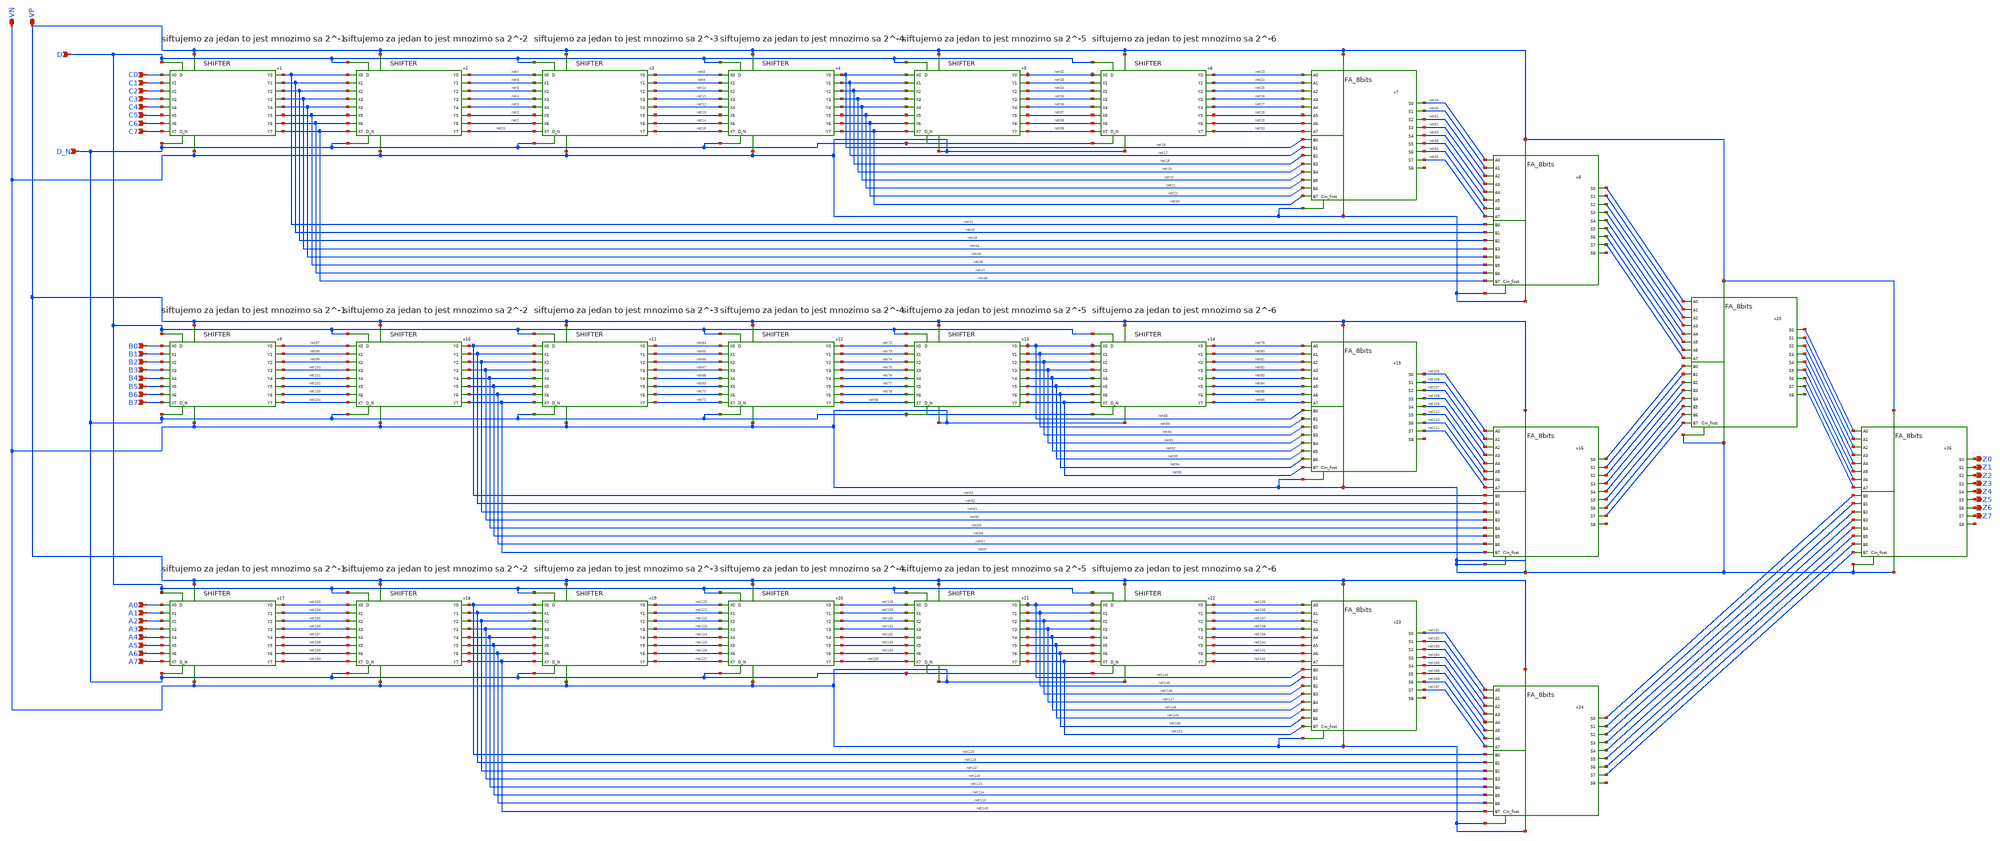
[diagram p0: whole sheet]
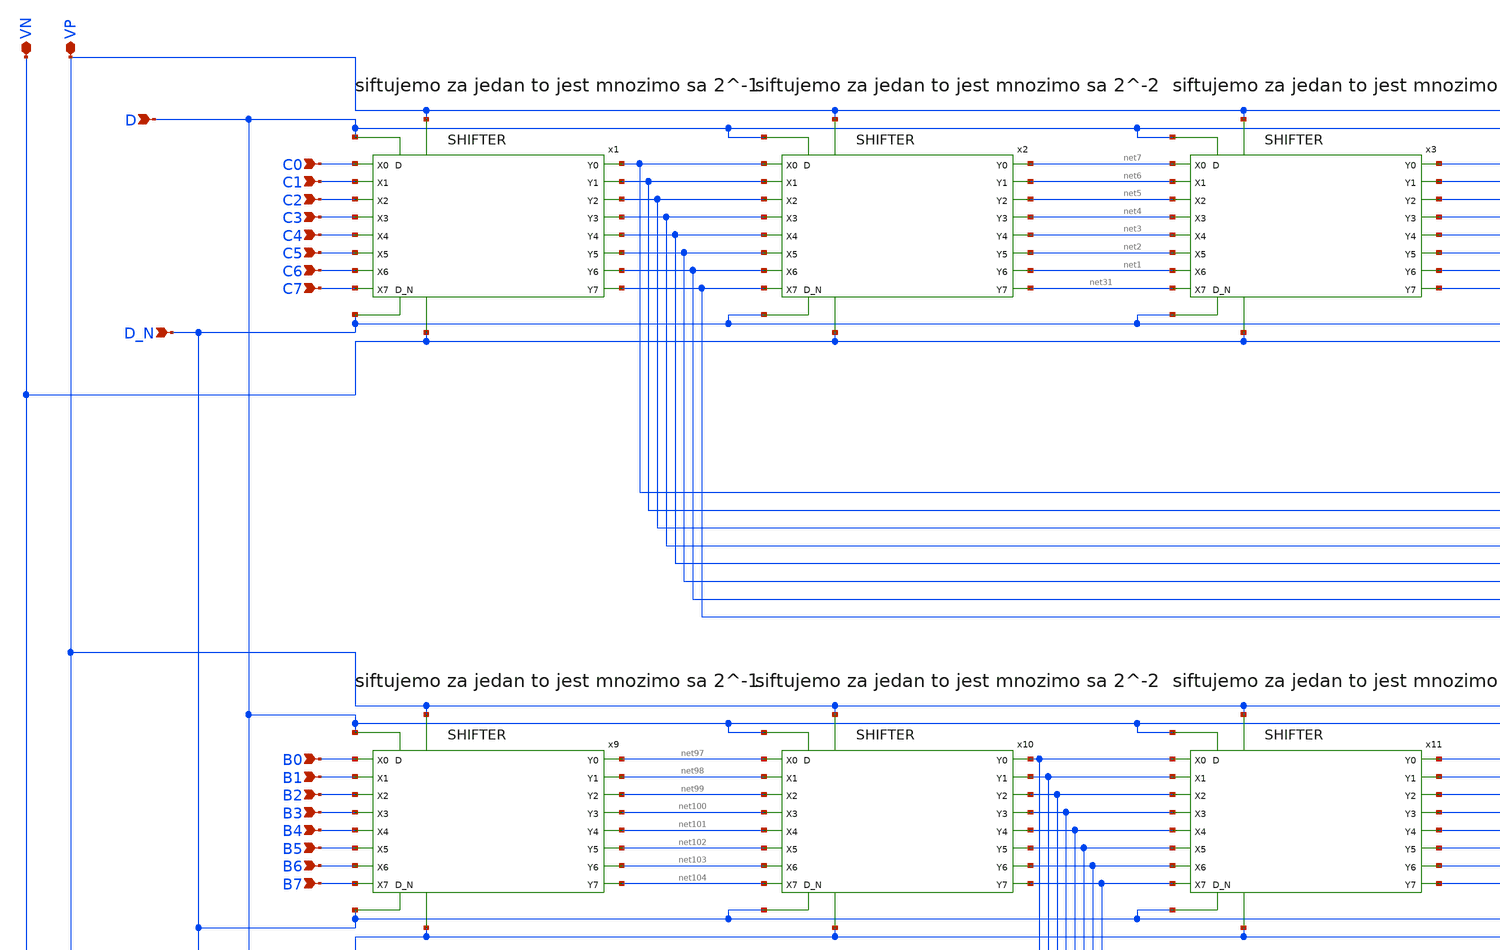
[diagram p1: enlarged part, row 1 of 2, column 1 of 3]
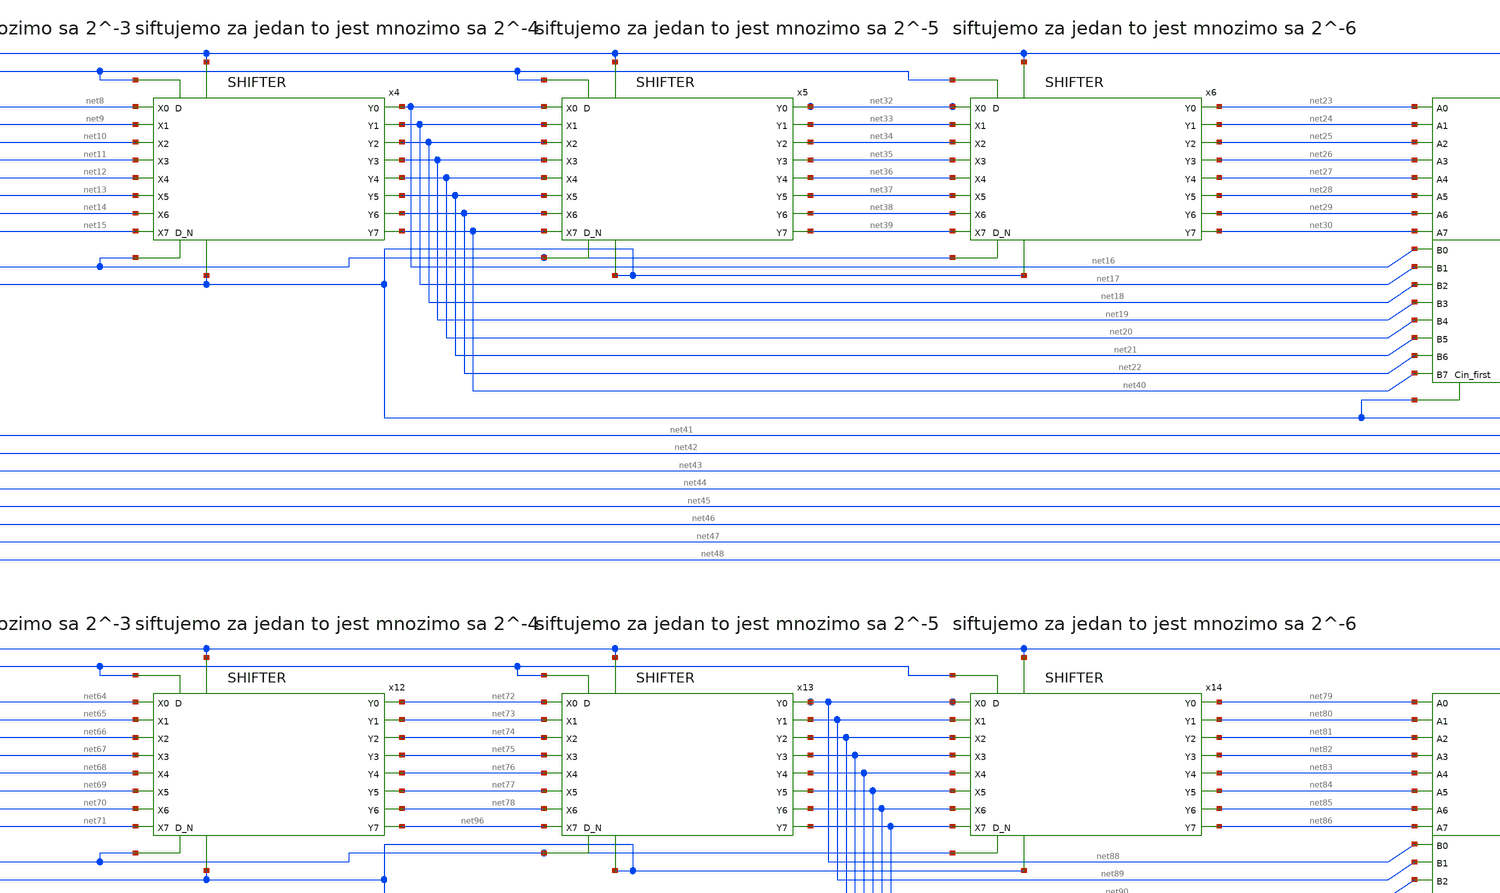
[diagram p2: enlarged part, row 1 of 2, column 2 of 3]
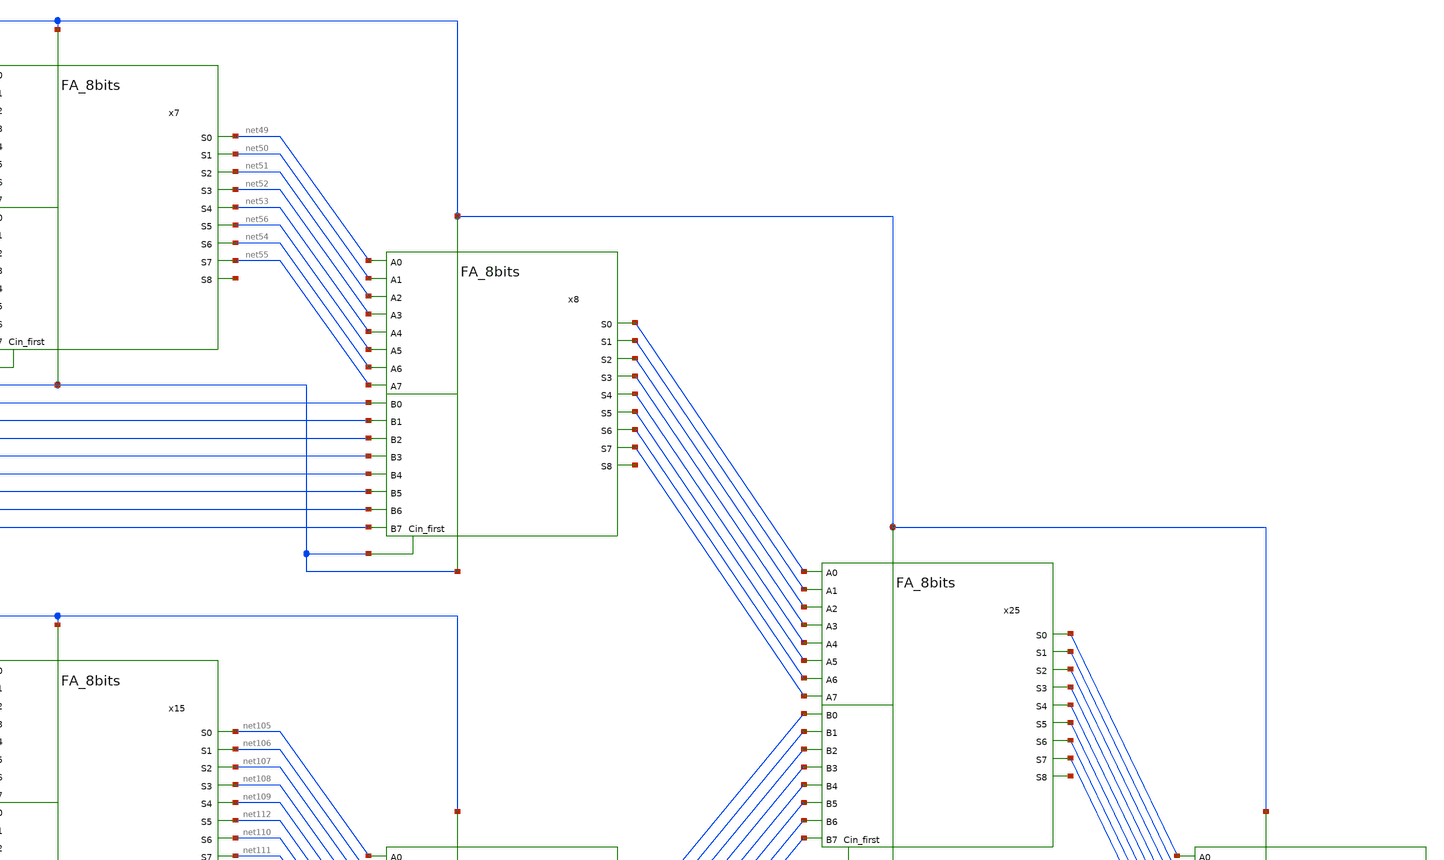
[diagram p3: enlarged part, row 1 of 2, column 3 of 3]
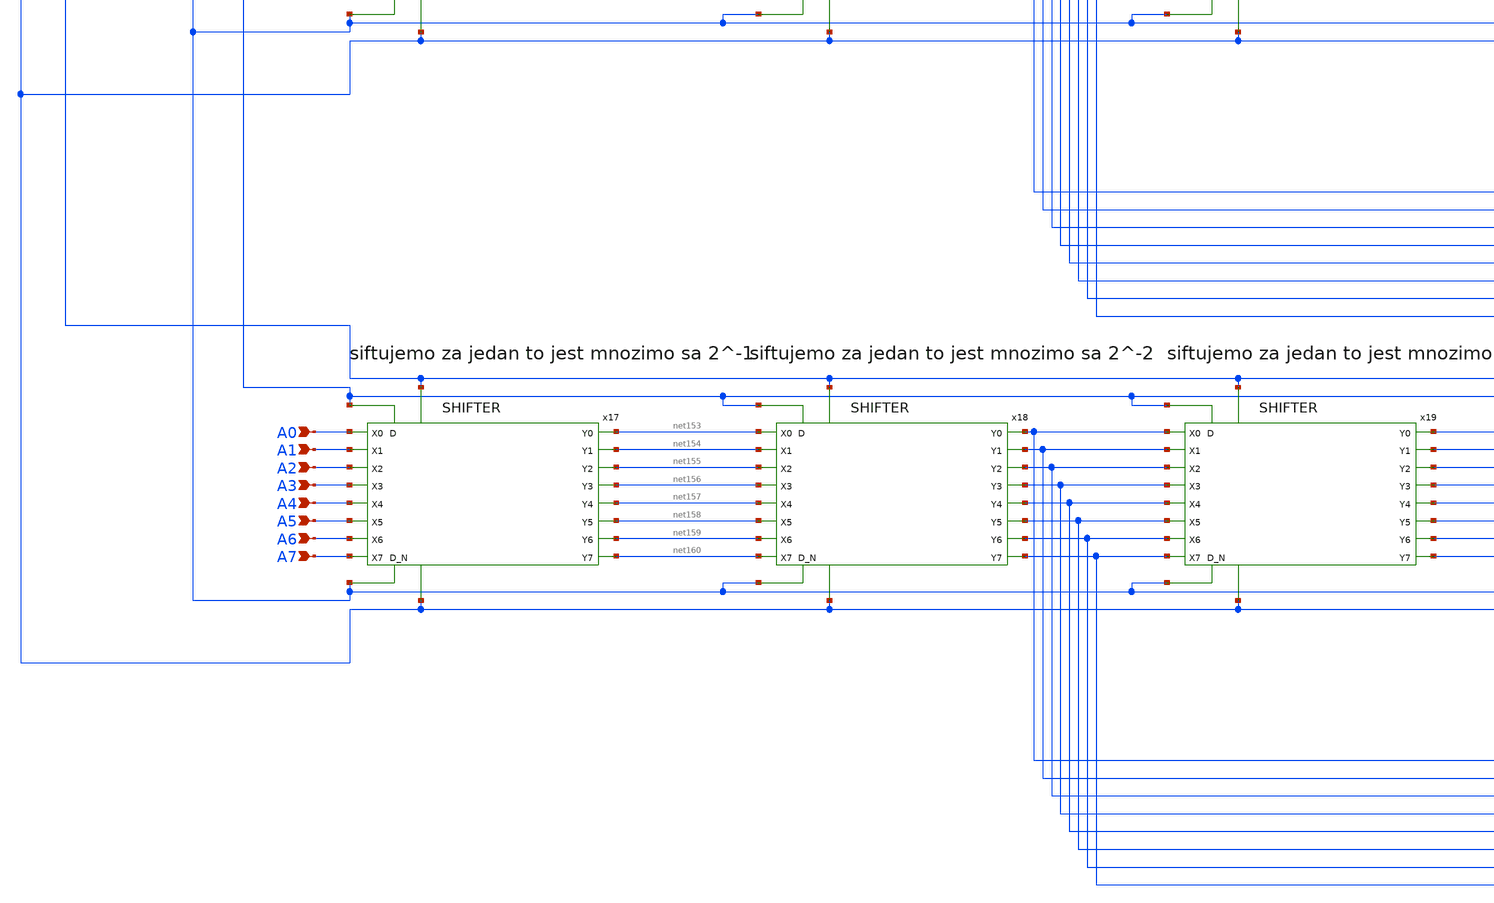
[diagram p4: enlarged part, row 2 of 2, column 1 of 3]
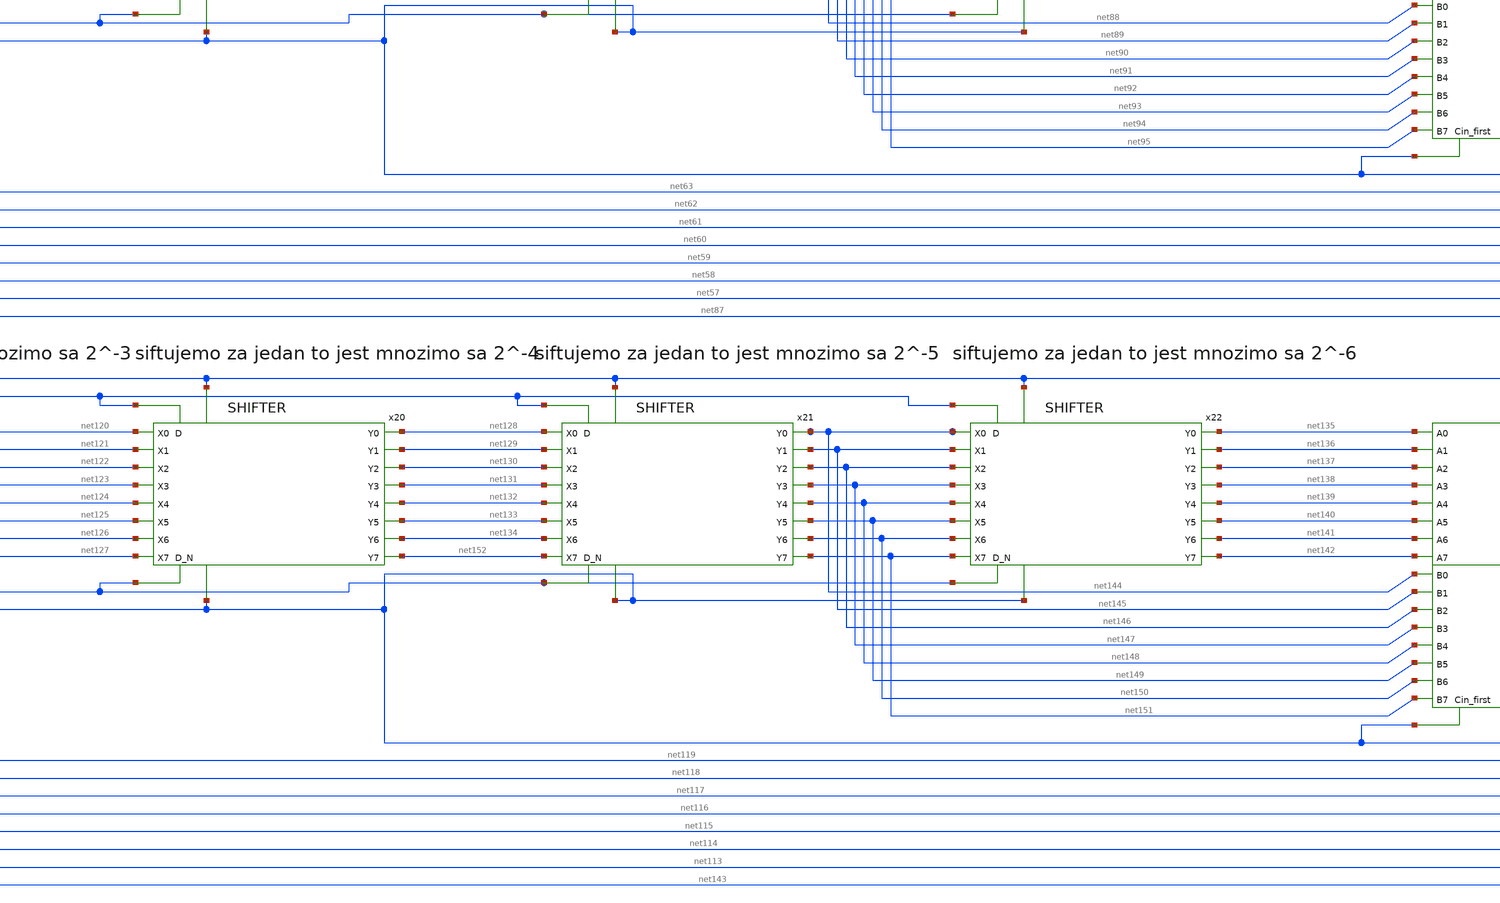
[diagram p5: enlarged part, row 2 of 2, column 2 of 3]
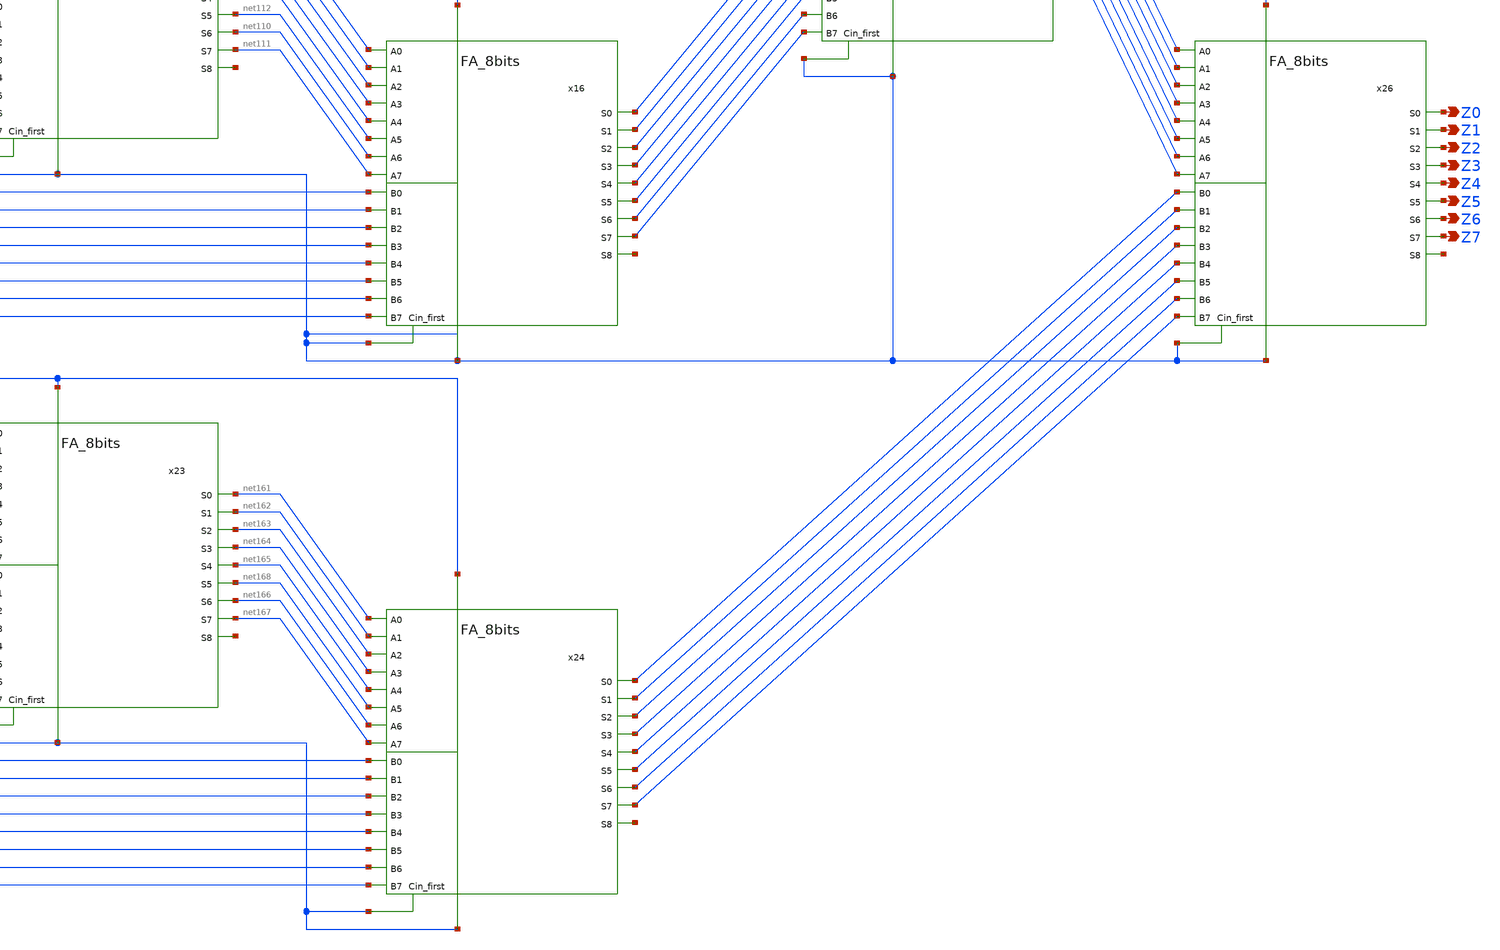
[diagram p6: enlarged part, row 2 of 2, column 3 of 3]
** sch_path: projekat_spice/layout/fir/FIR.sch
* projekat_spice/layout/fa/FA.sym:
* Copyright 2022 Stefan Frederik Schippers
* Licensed under the Apache License, Version 2.0 (the "License");
**.subckt FIR C0 C1 C2 C3 C4 C5 C6 C7 VP VN D D_N Z0 Z1 Z2 Z3 Z4 Z5 Z6 Z7 B0 B1 B2 B3 B4 B5 B6 B7 A0
*+ A1 A2 A3 A4 A5 A6 A7
*.ipin C0
*.ipin C1
*.ipin C2
*.ipin C3
*.ipin C4
*.ipin C5
*.ipin C6
*.ipin C7
*.iopin VP
*.iopin VN
*.ipin D
*.ipin D_N
*.opin Z0
*.opin Z1
*.opin Z2
*.opin Z3
*.opin Z4
*.opin Z5
*.opin Z6
*.opin Z7
*.ipin B0
*.ipin B1
*.ipin B2
*.ipin B3
*.ipin B4
*.ipin B5
*.ipin B6
*.ipin B7
*.ipin A0
*.ipin A1
*.ipin A2
*.ipin A3
*.ipin A4
*.ipin A5
*.ipin A6
*.ipin A7
x1 C0 net41 net42 C1 net43 C2 C3 net44 net45 C4 C5 net46 net47 C6 net48 C7 D D_N VP VN SHIFTER
x2 net41 net7 net6 net42 net5 net43 net44 net4 net3 net45 net46 net2 net1 net47 net31 net48 D D_N VP
+ VN SHIFTER
x3 net7 net8 net9 net6 net10 net5 net4 net11 net12 net3 net2 net13 net14 net1 net15 net31 D D_N VP
+ VN SHIFTER
x4 net8 net16 net17 net9 net18 net10 net11 net19 net20 net12 net13 net21 net22 net14 net40 net15 D
+ D_N VP VN SHIFTER
x5 net16 net32 net33 net17 net34 net18 net19 net35 net36 net20 net21 net37 net38 net22 net39 net40 D
+ D_N VP VN SHIFTER
x6 net32 net23 net24 net33 net25 net34 net35 net26 net27 net36 net37 net28 net29 net38 net30 net39 D
+ D_N VP VN SHIFTER
x7 net16 net17 net18 net19 net20 net21 net22 net40 net23 net24 net25 net26 net27 net28 net29 net30
+ net49 net50 net51 net52 net53 net56 net54 net55 net201 VN VP VN FA_8bits
x8 net41 net42 net43 net44 net45 net46 net47 net48 net49 net50 net51 net52 net53 net56 net54 net55
+ net169 net170 net172 net171 net173 net174 net175 net176 net202 VN VP VN FA_8bits
x9 B0 net97 net98 B1 net99 B2 B3 net100 net101 B4 B5 net102 net103 B6 net104 B7 D D_N VP VN SHIFTER
x10 net97 net63 net62 net98 net61 net99 net100 net60 net59 net101 net102 net58 net57 net103 net87
+ net104 D D_N VP VN SHIFTER
x11 net63 net64 net65 net62 net66 net61 net60 net67 net68 net59 net58 net69 net70 net57 net71 net87
+ D D_N VP VN SHIFTER
x12 net64 net72 net73 net65 net74 net66 net67 net75 net76 net68 net69 net77 net78 net70 net96 net71
+ D D_N VP VN SHIFTER
x13 net72 net88 net89 net73 net90 net74 net75 net91 net92 net76 net77 net93 net94 net78 net95 net96
+ D D_N VP VN SHIFTER
x14 net88 net79 net80 net89 net81 net90 net91 net82 net83 net92 net93 net84 net85 net94 net86 net95
+ D D_N VP VN SHIFTER
x15 net88 net89 net90 net91 net92 net93 net94 net95 net79 net80 net81 net82 net83 net84 net85 net86
+ net105 net106 net107 net108 net109 net112 net110 net111 net203 VN VP VN FA_8bits
x16 net63 net62 net61 net60 net59 net58 net57 net87 net105 net106 net107 net108 net109 net112 net110
+ net111 net177 net178 net179 net180 net181 net182 net183 net184 net204 VN VP VN FA_8bits
x17 A0 net153 net154 A1 net155 A2 A3 net156 net157 A4 A5 net158 net159 A6 net160 A7 D D_N VP VN
+ SHIFTER
x18 net153 net119 net118 net154 net117 net155 net156 net116 net115 net157 net158 net114 net113
+ net159 net143 net160 D D_N VP VN SHIFTER
x19 net119 net120 net121 net118 net122 net117 net116 net123 net124 net115 net114 net125 net126
+ net113 net127 net143 D D_N VP VN SHIFTER
x20 net120 net128 net129 net121 net130 net122 net123 net131 net132 net124 net125 net133 net134
+ net126 net152 net127 D D_N VP VN SHIFTER
x21 net128 net144 net145 net129 net146 net130 net131 net147 net148 net132 net133 net149 net150
+ net134 net151 net152 D D_N VP VN SHIFTER
x22 net144 net135 net136 net145 net137 net146 net147 net138 net139 net148 net149 net140 net141
+ net150 net142 net151 D D_N VP VN SHIFTER
x23 net144 net145 net146 net147 net148 net149 net150 net151 net135 net136 net137 net138 net139
+ net140 net141 net142 net161 net162 net163 net164 net165 net168 net166 net167 net205 VN VP VN FA_8bits
x24 net119 net118 net117 net116 net115 net114 net113 net143 net161 net162 net163 net164 net165
+ net168 net166 net167 net193 net194 net195 net196 net197 net198 net199 net200 net206 VN VP VN FA_8bits
x25 net177 net178 net179 net180 net181 net182 net183 net184 net169 net170 net172 net171 net173
+ net174 net175 net176 net185 net186 net187 net188 net189 net190 net191 net192 net207 VN VP VN FA_8bits
x26 net193 net194 net195 net196 net197 net198 net199 net200 net185 net186 net187 net188 net189
+ net190 net191 net192 Z0 Z1 Z2 Z3 Z4 Z5 Z6 Z7 net208 VN VP VN FA_8bits
**.ends

* expanding   symbol:  /home/mihailo/projekat_sky130/projekat_layout/shifter/SHIFTER.sym # of
*+ pins=20
** sym_path: projekat_spice/layout/shifter/SHIFTER.sym
** sch_path: projekat_spice/layout/shifter/SHIFTER.sch
.subckt SHIFTER X0 Y0 Y1 X1 Y2 X2 X3 Y3 Y4 X4 X5 Y5 Y6 X6 Y7 X7 D D_N VP VN
*.iopin VP
*.iopin VN
*.ipin X0
*.ipin X1
*.ipin X2
*.ipin X3
*.ipin X4
*.ipin X5
*.ipin X6
*.ipin X7
*.ipin D
*.ipin D_N
*.opin Y0
*.opin Y1
*.opin Y2
*.opin Y3
*.opin Y4
*.opin Y5
*.opin Y6
*.opin Y7
X1 X0 D net1 VP VN AND
X3 D_N X1 Y0 VP VN AND
X4 X1 D net2 VP VN AND
X5 D_N X2 net3 VP VN AND
X6 X2 D net4 VP VN AND
X7 D_N X3 net5 VP VN AND
X8 X3 D net6 VP VN AND
X9 D_N X4 net7 VP VN AND
X10 X4 D net8 VP VN AND
X11 D_N X5 net9 VP VN AND
X12 X5 D net10 VP VN AND
X13 D_N X6 net11 VP VN AND
X14 X6 D Y7 VP VN AND
X15 D_N X7 net12 VP VN AND
X2 net1 net3 Y1 VP VN OR
X16 net2 net5 Y2 VP VN OR
X17 net4 net7 Y3 VP VN OR
X18 net6 net9 Y4 VP VN OR
X19 net8 net11 Y5 VP VN OR
X20 net10 net12 Y6 VP VN OR
.ends


* expanding   symbol:  /home/mihailo/projekat_sky130/projekat_layout/fa_8bits/FA_8bits.sym # of
*+ pins=28
** sym_path: projekat_spice/layout/fa_8bits/FA_8bits.sym
** sch_path: projekat_spice/layout/fa_8bits/FA_8bits.sch
.subckt FA_8bits B0 B1 B2 B3 B4 B5 B6 B7 A0 A1 A2 A3 A4 A5 A6 A7 S0 S1 S2 S3 S4 S5 S6 S7 S8
+ Cin_first VP VN
*.ipin A0
*.ipin B0
*.ipin A1
*.ipin B1
*.opin S0
*.opin S1
*.iopin VP
*.iopin VN
*.ipin Cin_first
*.ipin A2
*.ipin B2
*.opin S2
*.ipin A3
*.ipin B3
*.opin S3
*.ipin A4
*.ipin B4
*.opin S4
*.ipin A5
*.ipin B5
*.opin S5
*.ipin A6
*.ipin B6
*.opin S6
*.opin S7
*.ipin A7
*.ipin B7
*.opin S8
X1 A0 B0 Cin_first net1 S0 VP VN FA
X2 A1 B1 net1 net2 S1 VP VN FA
X3 A2 B2 net2 net3 S2 VP VN FA
X4 A3 B3 net3 net4 S3 VP VN FA
X5 A4 B4 net4 net5 S4 VP VN FA
X6 A5 B5 net5 net6 S5 VP VN FA
X7 A6 B6 net6 net7 S6 VP VN FA
X8 A7 B7 net7 S8 S7 VP VN FA
.ends


* expanding   symbol:  /home/mihailo/projekat_sky130/projekat_layout/and/AND.sym # of pins=5
** sym_path: projekat_spice/layout/and/AND.sym
** sch_path: projekat_spice/layout/and/AND.sch
.subckt AND A B X VP VN
*.ipin A
*.ipin B
*.iopin VN
*.iopin VP
*.opin X
XM1 net1 A net2 VN sky130_fd_pr__nfet_01v8 L=0.15 W=1 nf=1 ad='int((nf+1)/2) * W/nf * 0.29' as='int((nf+2)/2) * W/nf * 0.29'
+ pd='2*int((nf+1)/2) * (W/nf + 0.29)' ps='2*int((nf+2)/2) * (W/nf + 0.29)' nrd='0.29 / W' nrs='0.29 / W'
+ sa=0 sb=0 sd=0 mult=1 m=1
XM2 net1 A VP VP sky130_fd_pr__pfet_01v8 L=0.15 W=1 nf=1 ad='int((nf+1)/2) * W/nf * 0.29' as='int((nf+2)/2) * W/nf * 0.29'
+ pd='2*int((nf+1)/2) * (W/nf + 0.29)' ps='2*int((nf+2)/2) * (W/nf + 0.29)' nrd='0.29 / W' nrs='0.29 / W'
+ sa=0 sb=0 sd=0 mult=1 m=1
XM3 net1 B VP VP sky130_fd_pr__pfet_01v8 L=0.15 W=1 nf=1 ad='int((nf+1)/2) * W/nf * 0.29' as='int((nf+2)/2) * W/nf * 0.29'
+ pd='2*int((nf+1)/2) * (W/nf + 0.29)' ps='2*int((nf+2)/2) * (W/nf + 0.29)' nrd='0.29 / W' nrs='0.29 / W'
+ sa=0 sb=0 sd=0 mult=1 m=1
XM4 net2 B VN VN sky130_fd_pr__nfet_01v8 L=0.15 W=1 nf=1 ad='int((nf+1)/2) * W/nf * 0.29' as='int((nf+2)/2) * W/nf * 0.29'
+ pd='2*int((nf+1)/2) * (W/nf + 0.29)' ps='2*int((nf+2)/2) * (W/nf + 0.29)' nrd='0.29 / W' nrs='0.29 / W'
+ sa=0 sb=0 sd=0 mult=1 m=1
XM5 X net1 VN VN sky130_fd_pr__nfet_01v8 L=0.15 W=1 nf=1 ad='int((nf+1)/2) * W/nf * 0.29' as='int((nf+2)/2) * W/nf * 0.29'
+ pd='2*int((nf+1)/2) * (W/nf + 0.29)' ps='2*int((nf+2)/2) * (W/nf + 0.29)' nrd='0.29 / W' nrs='0.29 / W'
+ sa=0 sb=0 sd=0 mult=1 m=1
XM6 X net1 VP VP sky130_fd_pr__pfet_01v8 L=0.15 W=1 nf=1 ad='int((nf+1)/2) * W/nf * 0.29' as='int((nf+2)/2) * W/nf * 0.29'
+ pd='2*int((nf+1)/2) * (W/nf + 0.29)' ps='2*int((nf+2)/2) * (W/nf + 0.29)' nrd='0.29 / W' nrs='0.29 / W'
+ sa=0 sb=0 sd=0 mult=1 m=1
.ends


* expanding   symbol:  /home/mihailo/projekat_sky130/projekat_layout/or/OR.sym # of pins=5
** sym_path: projekat_spice/layout/or/OR.sym
** sch_path: projekat_spice/layout/or/OR.sch
.subckt OR A B X VP VN
*.opin X
*.ipin A
*.ipin B
*.iopin VP
*.iopin VN
XM1 net2 A VN VN sky130_fd_pr__nfet_01v8 L=0.15 W=1 nf=1 ad='int((nf+1)/2) * W/nf * 0.29' as='int((nf+2)/2) * W/nf * 0.29'
+ pd='2*int((nf+1)/2) * (W/nf + 0.29)' ps='2*int((nf+2)/2) * (W/nf + 0.29)' nrd='0.29 / W' nrs='0.29 / W'
+ sa=0 sb=0 sd=0 mult=1 m=1
XM2 net1 A VP VP sky130_fd_pr__pfet_01v8 L=0.15 W=1 nf=1 ad='int((nf+1)/2) * W/nf * 0.29' as='int((nf+2)/2) * W/nf * 0.29'
+ pd='2*int((nf+1)/2) * (W/nf + 0.29)' ps='2*int((nf+2)/2) * (W/nf + 0.29)' nrd='0.29 / W' nrs='0.29 / W'
+ sa=0 sb=0 sd=0 mult=1 m=1
XM3 net2 B net1 VP sky130_fd_pr__pfet_01v8 L=0.15 W=1 nf=1 ad='int((nf+1)/2) * W/nf * 0.29' as='int((nf+2)/2) * W/nf * 0.29'
+ pd='2*int((nf+1)/2) * (W/nf + 0.29)' ps='2*int((nf+2)/2) * (W/nf + 0.29)' nrd='0.29 / W' nrs='0.29 / W'
+ sa=0 sb=0 sd=0 mult=1 m=1
XM4 net2 B VN VN sky130_fd_pr__nfet_01v8 L=0.15 W=1 nf=1 ad='int((nf+1)/2) * W/nf * 0.29' as='int((nf+2)/2) * W/nf * 0.29'
+ pd='2*int((nf+1)/2) * (W/nf + 0.29)' ps='2*int((nf+2)/2) * (W/nf + 0.29)' nrd='0.29 / W' nrs='0.29 / W'
+ sa=0 sb=0 sd=0 mult=1 m=1
XM5 X net2 VN VN sky130_fd_pr__nfet_01v8 L=0.15 W=1 nf=1 ad='int((nf+1)/2) * W/nf * 0.29' as='int((nf+2)/2) * W/nf * 0.29'
+ pd='2*int((nf+1)/2) * (W/nf + 0.29)' ps='2*int((nf+2)/2) * (W/nf + 0.29)' nrd='0.29 / W' nrs='0.29 / W'
+ sa=0 sb=0 sd=0 mult=1 m=1
XM6 X net2 VP VP sky130_fd_pr__pfet_01v8 L=0.15 W=1 nf=1 ad='int((nf+1)/2) * W/nf * 0.29' as='int((nf+2)/2) * W/nf * 0.29'
+ pd='2*int((nf+1)/2) * (W/nf + 0.29)' ps='2*int((nf+2)/2) * (W/nf + 0.29)' nrd='0.29 / W' nrs='0.29 / W'
+ sa=0 sb=0 sd=0 mult=1 m=1
.ends


* expanding   symbol:  /home/mihailo/projekat_sky130/projekat_layout/fa/FA.sym # of pins=7
** sym_path: projekat_spice/layout/fa/FA.sym
** sch_path: projekat_spice/layout/fa/FA.sch
.subckt FA A B Cin Out Sum VP VN
*.ipin A
*.opin Sum
*.iopin VP
*.iopin VN
*.opin Out
*.ipin B
*.ipin Cin
X4 A B VN VP net1 XOR
X5 Cin net1 VN VP Sum XOR
X1 Cin net1 net3 VP VN AND
X2 A B net2 VP VN AND
X3 net3 net2 Out VP VN OR
.ends


* expanding   symbol:  /home/mihailo/projekat_sky130/projekat_layout/xor/XOR.sym # of pins=5
** sym_path: projekat_spice/layout/xor/XOR.sym
** sch_path: projekat_spice/layout/xor/XOR.sch
.subckt XOR A B VN VP X
*.ipin A
*.ipin B
*.opin X
*.iopin VN
*.iopin VP
X1 B net3 net1 VP VN AND
X2 net4 A net2 VP VN AND
X3 net1 net2 X VP VN OR
X4 A net3 VP VN invertor
X5 B net4 VP VN invertor
.ends


* expanding   symbol:  /home/mihailo/projekat_sky130/projekat_layout/invertor/invertor.sym # of
*+ pins=4
** sym_path: projekat_spice/layout/invertor/invertor.sym
** sch_path: projekat_spice/layout/invertor/invertor.sch
.subckt invertor A Y VP VN
*.iopin VP
*.iopin VN
*.ipin A
*.opin Y
XM1 Y A VN VN sky130_fd_pr__nfet_01v8 L=0.15 W=1 nf=1 ad='int((nf+1)/2) * W/nf * 0.29' as='int((nf+2)/2) * W/nf * 0.29'
+ pd='2*int((nf+1)/2) * (W/nf + 0.29)' ps='2*int((nf+2)/2) * (W/nf + 0.29)' nrd='0.29 / W' nrs='0.29 / W'
+ sa=0 sb=0 sd=0 mult=1 m=1
XM2 Y A VP VP sky130_fd_pr__pfet_01v8 L=0.15 W=1 nf=1 ad='int((nf+1)/2) * W/nf * 0.29' as='int((nf+2)/2) * W/nf * 0.29'
+ pd='2*int((nf+1)/2) * (W/nf + 0.29)' ps='2*int((nf+2)/2) * (W/nf + 0.29)' nrd='0.29 / W' nrs='0.29 / W'
+ sa=0 sb=0 sd=0 mult=1 m=1
.ends

.end
